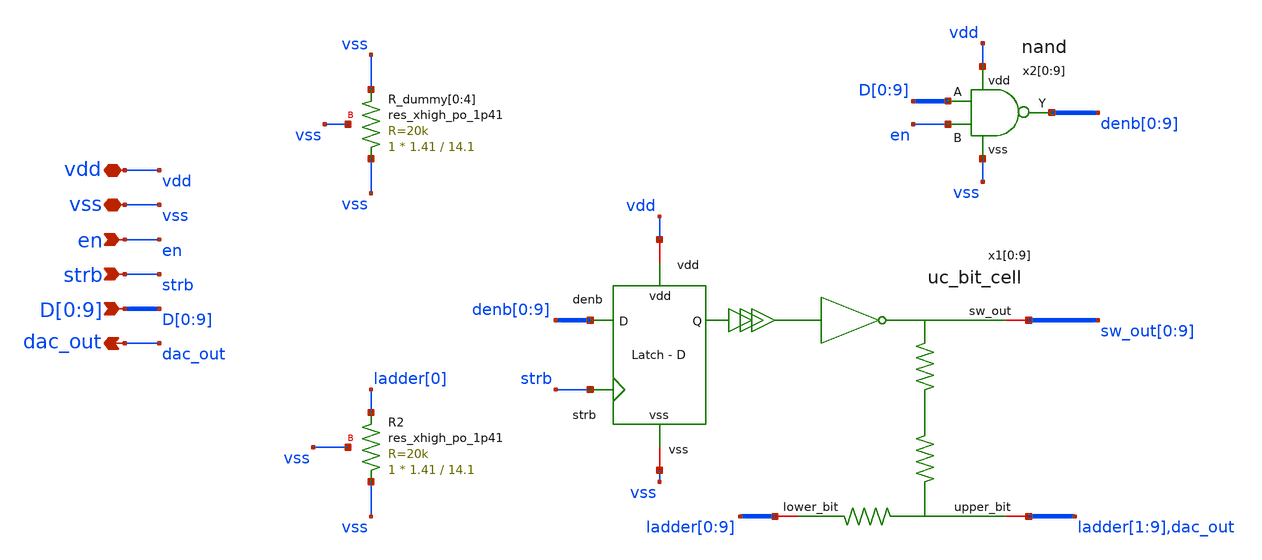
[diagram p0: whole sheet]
** sch_path: xschem/dac10b_top/dac10b_top.sch
**.subckt dac10b_top vdd vss en strb D[0],D[1],D[2],D[3],D[4],D[5],D[6],D[7],D[8],D[9] dac_out
*.iopin vdd
*.iopin vss
*.ipin en
*.ipin strb
*.ipin D[0],D[1],D[2],D[3],D[4],D[5],D[6],D[7],D[8],D[9]
*.opin dac_out
x1[0] denb[0] strb vdd vss ladder[0] ladder[1] sw_out[0] uc_bit_cell
x1[1] denb[1] strb vdd vss ladder[1] ladder[2] sw_out[1] uc_bit_cell
x1[2] denb[2] strb vdd vss ladder[2] ladder[3] sw_out[2] uc_bit_cell
x1[3] denb[3] strb vdd vss ladder[3] ladder[4] sw_out[3] uc_bit_cell
x1[4] denb[4] strb vdd vss ladder[4] ladder[5] sw_out[4] uc_bit_cell
x1[5] denb[5] strb vdd vss ladder[5] ladder[6] sw_out[5] uc_bit_cell
x1[6] denb[6] strb vdd vss ladder[6] ladder[7] sw_out[6] uc_bit_cell
x1[7] denb[7] strb vdd vss ladder[7] ladder[8] sw_out[7] uc_bit_cell
x1[8] denb[8] strb vdd vss ladder[8] ladder[9] sw_out[8] uc_bit_cell
x1[9] denb[9] strb vdd vss ladder[9] dac_out sw_out[9] uc_bit_cell
x2[0] vdd vss D[0] en denb[0] nand
x2[1] vdd vss D[1] en denb[1] nand
x2[2] vdd vss D[2] en denb[2] nand
x2[3] vdd vss D[3] en denb[3] nand
x2[4] vdd vss D[4] en denb[4] nand
x2[5] vdd vss D[5] en denb[5] nand
x2[6] vdd vss D[6] en denb[6] nand
x2[7] vdd vss D[7] en denb[7] nand
x2[8] vdd vss D[8] en denb[8] nand
x2[9] vdd vss D[9] en denb[9] nand
XR2 vss ladder[0] vss sky130_fd_pr__res_xhigh_po_1p41 L=14.1 mult=1 m=1
XR_dummy[0] vss vss vss sky130_fd_pr__res_xhigh_po_1p41 L=14.1 mult=1 m=1
XR_dummy[1] vss vss vss sky130_fd_pr__res_xhigh_po_1p41 L=14.1 mult=1 m=1
XR_dummy[2] vss vss vss sky130_fd_pr__res_xhigh_po_1p41 L=14.1 mult=1 m=1
XR_dummy[3] vss vss vss sky130_fd_pr__res_xhigh_po_1p41 L=14.1 mult=1 m=1
XR_dummy[4] vss vss vss sky130_fd_pr__res_xhigh_po_1p41 L=14.1 mult=1 m=1
**.ends
.end
